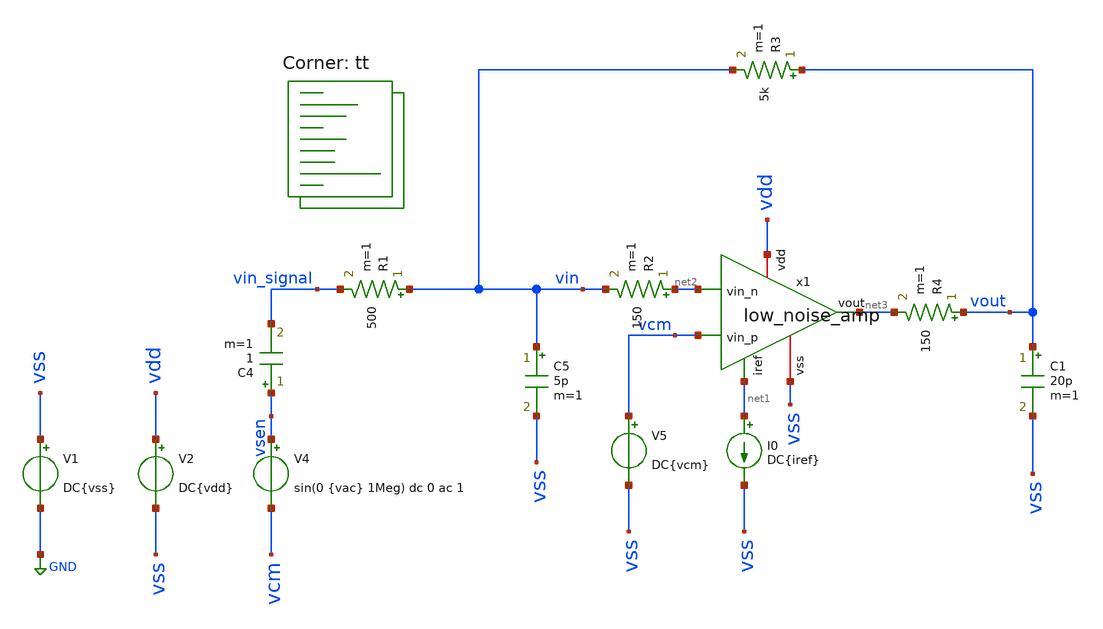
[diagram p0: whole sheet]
** sch_path: design/xschem/low_noise_amp_closed_loop_rpad_tb.sch
**.subckt low_noise_amp_closed_loop_rpad_tb
V1 vss GND DC{vss}
V2 vdd vss DC{vdd}
V4 vsen vcm sin(0 {vac} 1Meg) dc 0 ac 1
C4 vsen vin_signal 1 m=1
I0 net1 vss DC{iref}
R1 vin vin_signal 500 m=1
R3 vout vin 5k m=1
C5 vin vss 5p m=1
C1 vout vss 20p m=1
V5 vcm vss DC{vcm}
R2 net2 vin 150 m=1
R4 vout net3 150 m=1
x1 vdd net1 net2 vcm net3 vss low_noise_amp
**** begin user architecture code




* Circuit Parameters
.param iref = 100u
.param vdd  = 1.8
.param vss  = 0.0
.param vcm  = 0.8
.param vac  = 10m
.options TEMP = 65.0


* OP Parameters & Singals to save
.save all  @M.X1.XM1.msky130_fd_pr__pfet_01v8[id] @M.X1.XM1.msky130_fd_pr__pfet_01v8[vth] @M.X1.XM1.msky130_fd_pr__pfet_01v8[vgs] @M.X1.XM1.msky130_fd_pr__pfet_01v8[vds] @M.X1.XM1.msky130_fd_pr__pfet_01v8[vdsat] @M.X1.XM1.msky130_fd_pr__pfet_01v8[gm] @M.X1.XM1.msky130_fd_pr__pfet_01v8[gds]  @M.X1.XM2.msky130_fd_pr__pfet_01v8[id] @M.X1.XM2.msky130_fd_pr__pfet_01v8[vth] @M.X1.XM2.msky130_fd_pr__pfet_01v8[vgs] @M.X1.XM2.msky130_fd_pr__pfet_01v8[vds] @M.X1.XM2.msky130_fd_pr__pfet_01v8[vdsat] @M.X1.XM2.msky130_fd_pr__pfet_01v8[gm] @M.X1.XM2.msky130_fd_pr__pfet_01v8[gds]  @M.X1.XM3.msky130_fd_pr__nfet_01v8[id] @M.X1.XM3.msky130_fd_pr__nfet_01v8[vth] @M.X1.XM3.msky130_fd_pr__nfet_01v8[vgs] @M.X1.XM3.msky130_fd_pr__nfet_01v8[vds] @M.X1.XM3.msky130_fd_pr__nfet_01v8[vdsat] @M.X1.XM3.msky130_fd_pr__nfet_01v8[gm] @M.X1.XM3.msky130_fd_pr__nfet_01v8[gds]  @M.X1.XM4.msky130_fd_pr__nfet_01v8[id] @M.X1.XM4.msky130_fd_pr__nfet_01v8[vth] @M.X1.XM4.msky130_fd_pr__nfet_01v8[vgs] @M.X1.XM4.msky130_fd_pr__nfet_01v8[vds] @M.X1.XM4.msky130_fd_pr__nfet_01v8[vdsat] @M.X1.XM4.msky130_fd_pr__nfet_01v8[gm] @M.X1.XM4.msky130_fd_pr__nfet_01v8[gds]  @M.X1.XM5.msky130_fd_pr__pfet_01v8[id] @M.X1.XM5.msky130_fd_pr__pfet_01v8[vth] @M.X1.XM5.msky130_fd_pr__pfet_01v8[vgs] @M.X1.XM5.msky130_fd_pr__pfet_01v8[vds] @M.X1.XM5.msky130_fd_pr__pfet_01v8[vdsat] @M.X1.XM5.msky130_fd_pr__pfet_01v8[gm] @M.X1.XM5.msky130_fd_pr__pfet_01v8[gds]  @M.X1.XM6.msky130_fd_pr__nfet_01v8[id] @M.X1.XM6.msky130_fd_pr__nfet_01v8[vth] @M.X1.XM6.msky130_fd_pr__nfet_01v8[vgs] @M.X1.XM6.msky130_fd_pr__nfet_01v8[vds] @M.X1.XM6.msky130_fd_pr__nfet_01v8[vdsat] @M.X1.XM6.msky130_fd_pr__nfet_01v8[gm] @M.X1.XM6.msky130_fd_pr__nfet_01v8[gds]  @M.X1.XM7.msky130_fd_pr__pfet_01v8[id] @M.X1.XM7.msky130_fd_pr__pfet_01v8[vth] @M.X1.XM7.msky130_fd_pr__pfet_01v8[vgs] @M.X1.XM7.msky130_fd_pr__pfet_01v8[vds] @M.X1.XM7.msky130_fd_pr__pfet_01v8[vdsat] @M.X1.XM7.msky130_fd_pr__pfet_01v8[gm] @M.X1.XM7.msky130_fd_pr__pfet_01v8[gds]  @M.X1.XM8.msky130_fd_pr__pfet_01v8[id] @M.X1.XM8.msky130_fd_pr__pfet_01v8[vth] @M.X1.XM8.msky130_fd_pr__pfet_01v8[vgs] @M.X1.XM8.msky130_fd_pr__pfet_01v8[vds] @M.X1.XM8.msky130_fd_pr__pfet_01v8[vdsat] @M.X1.XM8.msky130_fd_pr__pfet_01v8[gm] @M.X1.XM8.msky130_fd_pr__pfet_01v8[gds]  @M.X1.XM9.msky130_fd_pr__nfet_01v8[id] @M.X1.XM9.msky130_fd_pr__nfet_01v8[vth] @M.X1.XM9.msky130_fd_pr__nfet_01v8[vgs] @M.X1.XM9.msky130_fd_pr__nfet_01v8[vds] @M.X1.XM9.msky130_fd_pr__nfet_01v8[vdsat] @M.X1.XM9.msky130_fd_pr__nfet_01v8[gm] @M.X1.XM9.msky130_fd_pr__nfet_01v8[gds]

*Simulations
.control
  ac dec 100 1k 10G
  setplot ac1
  meas ac GBW when vdb(vout)=0
  meas ac DCG find vdb(vout) at=1k
  *meas ac PM find vp(vout) when vdb(vout)=0
  *print PM*180/PI
  *meas ac GM find vdb(vout) when vp(vout)=0
  plot vdb(vout) {vp(vout)*180/PI}
  *write opamp_closeloop_rpad_ac1.raw

  reset
  tran 0.01u 11u
  setplot tran1
  plot v(vsen) v(vout)
  *write opamp_closeloop_rpad_tran1.raw

  reset
  noise v(vout) V4 dec 100 1k 10G 1
  setplot noise1
  plot inoise_spectrum onoise_spectrum
  *print inoise_spectrum
  *print onoise_spectrum
  setplot noise2
  *plot inoise_total onoise_total
  print inoise_total
  print onoise_total
  *write opamp_closeloop_rpad_noise.raw

  reset
  op
  setplot op1
  print vout
  *write opamp_closeloop_rapd_op1.raw

.endc

.end


.lib $::SKYWATER_MODELS/sky130.lib.spice tt
**** end user architecture code
**.ends
.GLOBAL GND
.end
